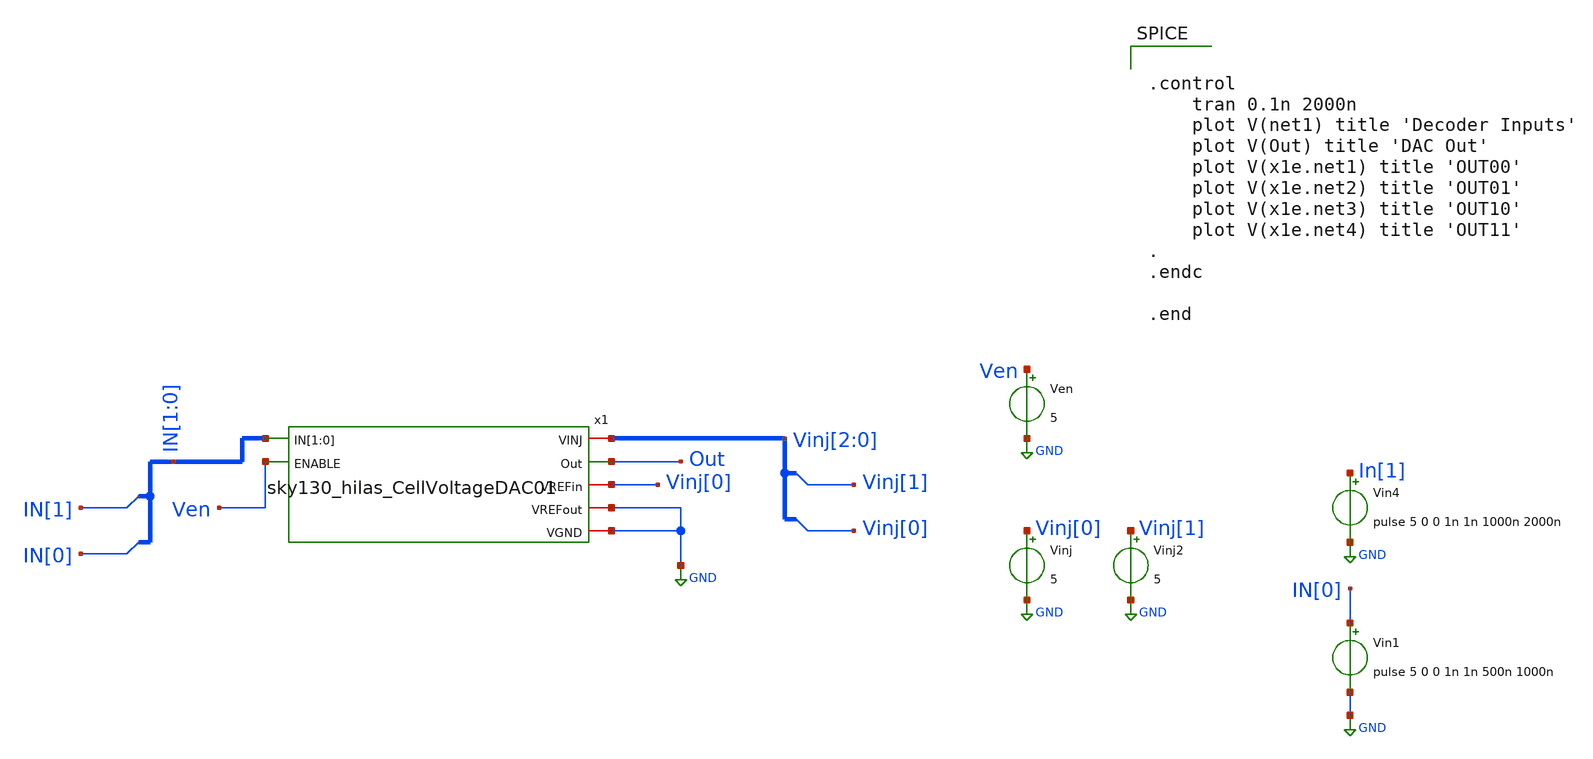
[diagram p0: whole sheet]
** sch_path: sky130_cells/RDAC/Sims/RDAC_cell_testbench.sch
**.subckt RDAC_cell_testbench
Vinj Vinj[0] GND 5
Ven Ven GND 5
Vin1 IN[0] GND pulse 5 0 0 1n 1n 500n 1000n
Vin4 In[1] GND pulse 5 0 0 1n 1n 1000n 2000n
Vinj2 Vinj[1] GND 5
x1 Vinj[2] IN[1] IN[0] Ven Out Vinj[0] GND GND sky130_hilas_CellVoltageDAC01
**** begin user architecture code


.control
	tran 0.1n 2000n
	plot V(net1) title 'Decoder Inputs'
	plot V(Out) title 'DAC Out'
	plot V(x1e.net1) title 'OUT00'
	plot V(x1e.net2) title 'OUT01'
	plot V(x1e.net3) title 'OUT10'
	plot V(x1e.net4) title 'OUT11'
.
.endc

.end


** opencircuitdesign pdks install
.lib $::SKYWATER_MODELS/sky130.lib.spice tt


**** end user architecture code
**.ends

* expanding   symbol:  sky130_cells/RDAC/Design/sky130_hilas_CellVoltageDAC01.sym # of pins=7
** sym_path: sky130_cells/RDAC/Design/sky130_hilas_CellVoltageDAC01.sym
** sch_path: sky130_cells/RDAC/Design/sky130_hilas_CellVoltageDAC01.sch
.subckt sky130_hilas_CellVoltageDAC01 VINJ IN[1] IN[0] ENABLE Out VREFin VREFout VGND
*.iopin VINJ
*.opin Out
*.iopin VREFout
*.ipin ENABLE
*.ipin IN[1],IN[0]
*.iopin VREFin
*.iopin VGND
x1 VINJ VREFin net1 net2 Out net3 net4 VGND VREFout sky130_hilas_dac_cell
x2 VINJ IN[1] IN[0] ENABLE net1 net2 net3 net4 VGND sky130_hilas_VinjDecode2to4
.ends


* expanding   symbol:  sky130_cells/RDAC/Design/sky130_hilas_dac_cell.sym # of pins=9
** sym_path: sky130_cells/RDAC/Design/sky130_hilas_dac_cell.sym
** sch_path: sky130_cells/RDAC/Design/sky130_hilas_dac_cell.sch
.subckt sky130_hilas_dac_cell VDD VREFin D0 D1 Out D2 D3 GND VREFout
*.iopin VDD
*.opin Out
*.ipin D0
*.ipin D1
*.ipin D2
*.ipin D3
*.iopin GND
*.iopin VREFout
*.iopin VREFin
x1 VDD Out D0 Node[0] GND Tgate
x2 VDD Out D1 Node[1] GND Tgate
x3 VDD Out D2 Node[2] GND Tgate
x4 VDD Out D3 Node[3] GND Tgate
x5 VREFin Node[3] Node[2] Node[1] Node[0] VREFout sky130_hilas_resistor_string
.ends


* expanding   symbol:  sky130_cells/RDAC/Design/sky130_hilas_VinjDecode2to4.sym # of pins=8
** sym_path: sky130_cells/RDAC/Design/sky130_hilas_VinjDecode2to4.sym
** sch_path: sky130_cells/RDAC/Design/sky130_hilas_VinjDecode2to4.sch
.subckt sky130_hilas_VinjDecode2to4 VINJ IN[1] IN[0] ENABLE OUTPUT00 OUTPUT01 OUTPUT10 OUTPUT11 VGND
*.ipin ENABLE
*.opin OUTPUT00
*.opin OUTPUT01
*.opin OUTPUT10
*.opin OUTPUT11
*.iopin VINJ
*.iopin VGND
*.ipin IN[1],IN[0]
x2 VINJ IN[1] VinjNOR3_2/Input2 VGND sky130_hilas_VinjInv2
x3 VINJ IN[0] VinjNOR3_1/Input1 VGND sky130_hilas_VinjInv2
x4 VINJ ENABLE VinjNOR3_3/Input3 VGND sky130_hilas_VinjInv2
x1 VINJ IN[1] IN[0] VinjNOR3_3/Input3 OUTPUT00 VGND sky130_hilas_VinjNOR3
x5 VINJ IN[1] VinjNOR3_1/Input1 VinjNOR3_3/Input3 OUTPUT01 VGND sky130_hilas_VinjNOR3
x6 VINJ VinjNOR3_2/Input2 IN[0] VinjNOR3_3/Input3 OUTPUT10 VGND sky130_hilas_VinjNOR3
x7 VINJ VinjNOR3_2/Input2 VinjNOR3_1/Input1 VinjNOR3_3/Input3 OUTPUT11 VGND sky130_hilas_VinjNOR3
.ends


* expanding   symbol:  sky130_cells/RDAC/Design/Tgate.sym # of pins=5
** sym_path: sky130_cells/RDAC/Design/Tgate.sym
** sch_path: sky130_cells/RDAC/Design/Tgate.sch
.subckt Tgate VINJ OUTPUT SELECT INPUT VGND
*.iopin VINJ
*.ipin SELECT
*.iopin INPUT
*.iopin OUTPUT
*.ipin VGND
XM5 net1 SELECT VGND VGND sky130_fd_pr__nfet_g5v0d10v5 L=0.5 W=0.42 nf=1 ad='int((1 + 1)/2) * 0.42 / 1 * 0.29'
+ as='int((1 + 2)/2) * 0.42 / 1 * 0.29' pd='2*int((1 + 1)/2) * (0.42 / 1 + 0.29)' ps='2*int((1 + 2)/2) * (0.42 / 1 + 0.29)'
+ nrd='0.29 / 0.42 ' nrs='0.29 / 0.42 ' sa=0 sb=0 sd=0 mult=1 m=1
XM1 net1 SELECT VINJ VINJ sky130_fd_pr__pfet_g5v0d10v5 L=0.5 W=0.42 nf=1 ad='int((1 + 1)/2) * 0.42 / 1 * 0.29'
+ as='int((1 + 2)/2) * 0.42 / 1 * 0.29' pd='2*int((1 + 1)/2) * (0.42 / 1 + 0.29)' ps='2*int((1 + 2)/2) * (0.42 / 1 + 0.29)'
+ nrd='0.29 / 0.42 ' nrs='0.29 / 0.42 ' sa=0 sb=0 sd=0 mult=1 m=1
XM2 INPUT net1 OUTPUT VINJ sky130_fd_pr__pfet_g5v0d10v5 L=0.5 W=0.42 nf=1 ad='int((1 + 1)/2) * 0.42 / 1 * 0.29'
+ as='int((1 + 2)/2) * 0.42 / 1 * 0.29' pd='2*int((1 + 1)/2) * (0.42 / 1 + 0.29)' ps='2*int((1 + 2)/2) * (0.42 / 1 + 0.29)'
+ nrd='0.29 / 0.42 ' nrs='0.29 / 0.42 ' sa=0 sb=0 sd=0 mult=1 m=1
XM3 OUTPUT SELECT INPUT VGND sky130_fd_pr__nfet_g5v0d10v5 L=0.5 W=0.42 nf=1 ad='int((1 + 1)/2) * 0.42 / 1 * 0.29'
+ as='int((1 + 2)/2) * 0.42 / 1 * 0.29' pd='2*int((1 + 1)/2) * (0.42 / 1 + 0.29)' ps='2*int((1 + 2)/2) * (0.42 / 1 + 0.29)'
+ nrd='0.29 / 0.42 ' nrs='0.29 / 0.42 ' sa=0 sb=0 sd=0 mult=1 m=1
.ends


* expanding   symbol:  sky130_cells/RDAC/Design/sky130_hilas_resistor_string.sym # of pins=3
** sym_path: sky130_cells/RDAC/Design/sky130_hilas_resistor_string.sym
** sch_path: sky130_cells/RDAC/Design/sky130_hilas_resistor_string.sch
.subckt sky130_hilas_resistor_string VREFin Node[3] Node[2] Node[1] Node[0] VREFout
*.iopin VREFout
*.iopin VREFin
*.opin Node[3],Node[2],Node[1],Node[0]
XR1 Node[0] VREFin sky130_fd_pr__res_generic_po W=0.33 L=10.19 m=1
XR2 net1 Node[0] sky130_fd_pr__res_generic_po W=0.33 L=10.19 m=1
XR3 Node[1] net1 sky130_fd_pr__res_generic_po W=0.33 L=10.19 m=1
XR4 net2 Node[1] sky130_fd_pr__res_generic_po W=0.33 L=10.19 m=1
XR5 Node[2] net2 sky130_fd_pr__res_generic_po W=0.33 L=10.19 m=1
XR6 net3 Node[2] sky130_fd_pr__res_generic_po W=0.33 L=10.19 m=1
XR7 Node[3] net3 sky130_fd_pr__res_generic_po W=0.33 L=10.19 m=1
XR8 VREFout Node[3] sky130_fd_pr__res_generic_po W=0.33 L=10.19 m=1
.ends


* expanding   symbol:  sky130_cells/RDAC/Design/sky130_hilas_VinjInv2.sym # of pins=4
** sym_path: sky130_cells/RDAC/Design/sky130_hilas_VinjInv2.sym
** sch_path: sky130_cells/RDAC/Design/sky130_hilas_VinjInv2.sch
.subckt sky130_hilas_VinjInv2 Vinj Input Output GND
*.ipin Input
*.opin Output
*.iopin Vinj
*.iopin GND
XM4 Output Input Vinj Vinj sky130_fd_pr__pfet_g5v0d10v5 L=0.53 W=0.42 nf=1 ad='int((nf+1)/2) * W/nf * 0.29'
+ as='int((nf+2)/2) * W/nf * 0.29' pd='2*int((nf+1)/2) * (W/nf + 0.29)' ps='2*int((nf+2)/2) * (W/nf + 0.29)'
+ nrd='0.29 / W' nrs='0.29 / W' sa=0 sb=0 sd=0 mult=1 m=1
XM3 Output Input GND GND sky130_fd_pr__nfet_g5v0d10v5 L=0.52 W=0.42 nf=1 ad='int((nf+1)/2) * W/nf * 0.29'
+ as='int((nf+2)/2) * W/nf * 0.29' pd='2*int((nf+1)/2) * (W/nf + 0.29)' ps='2*int((nf+2)/2) * (W/nf + 0.29)'
+ nrd='0.29 / W' nrs='0.29 / W' sa=0 sb=0 sd=0 mult=1 m=1
.ends


* expanding   symbol:  sky130_cells/RDAC/Design/sky130_hilas_VinjNOR3.sym # of pins=6
** sym_path: sky130_cells/RDAC/Design/sky130_hilas_VinjNOR3.sym
** sch_path: sky130_cells/RDAC/Design/sky130_hilas_VinjNOR3.sch
.subckt sky130_hilas_VinjNOR3 Vinj Input1 Input2 Input3 OUTPUT GND
*.ipin Input3
*.ipin Input1
*.ipin Input2
*.iopin Vinj
*.iopin GND
*.opin OUTPUT
XM1 OUTPUT Input3 GND GND sky130_fd_pr__nfet_g5v0d10v5 L=0.5 W=0.42 nf=1 ad='int((nf+1)/2) * W/nf * 0.29'
+ as='int((nf+2)/2) * W/nf * 0.29' pd='2*int((nf+1)/2) * (W/nf + 0.29)' ps='2*int((nf+2)/2) * (W/nf + 0.29)'
+ nrd='0.29 / W' nrs='0.29 / W' sa=0 sb=0 sd=0 mult=1 m=1
XM2 OUTPUT Input1 GND GND sky130_fd_pr__nfet_g5v0d10v5 L=0.51 W=0.43 nf=1 ad='int((nf+1)/2) * W/nf * 0.29'
+ as='int((nf+2)/2) * W/nf * 0.29' pd='2*int((nf+1)/2) * (W/nf + 0.29)' ps='2*int((nf+2)/2) * (W/nf + 0.29)'
+ nrd='0.29 / W' nrs='0.29 / W' sa=0 sb=0 sd=0 mult=1 m=1
XM3 OUTPUT Input2 GND GND sky130_fd_pr__nfet_g5v0d10v5 L=0.5 W=0.42 nf=1 ad='int((nf+1)/2) * W/nf * 0.29'
+ as='int((nf+2)/2) * W/nf * 0.29' pd='2*int((nf+1)/2) * (W/nf + 0.29)' ps='2*int((nf+2)/2) * (W/nf + 0.29)'
+ nrd='0.29 / W' nrs='0.29 / W' sa=0 sb=0 sd=0 mult=1 m=1
XM6 OUTPUT Input2 net2 Vinj sky130_fd_pr__pfet_g5v0d10v5 L=0.52 W=0.43 nf=1 ad='int((nf+1)/2) * W/nf * 0.29'
+ as='int((nf+2)/2) * W/nf * 0.29' pd='2*int((nf+1)/2) * (W/nf + 0.29)' ps='2*int((nf+2)/2) * (W/nf + 0.29)'
+ nrd='0.29 / W' nrs='0.29 / W' sa=0 sb=0 sd=0 mult=1 m=1
XM4 net2 Input1 net1 Vinj sky130_fd_pr__pfet_g5v0d10v5 L=0.52 W=0.42 nf=1 ad='int((nf+1)/2) * W/nf * 0.29'
+ as='int((nf+2)/2) * W/nf * 0.29' pd='2*int((nf+1)/2) * (W/nf + 0.29)' ps='2*int((nf+2)/2) * (W/nf + 0.29)'
+ nrd='0.29 / W' nrs='0.29 / W' sa=0 sb=0 sd=0 mult=1 m=1
XM5 net1 Input3 Vinj Vinj sky130_fd_pr__pfet_g5v0d10v5 L=0.53 W=0.42 nf=1 ad='int((nf+1)/2) * W/nf * 0.29'
+ as='int((nf+2)/2) * W/nf * 0.29' pd='2*int((nf+1)/2) * (W/nf + 0.29)' ps='2*int((nf+2)/2) * (W/nf + 0.29)'
+ nrd='0.29 / W' nrs='0.29 / W' sa=0 sb=0 sd=0 mult=1 m=1
.ends

.GLOBAL GND
.end
